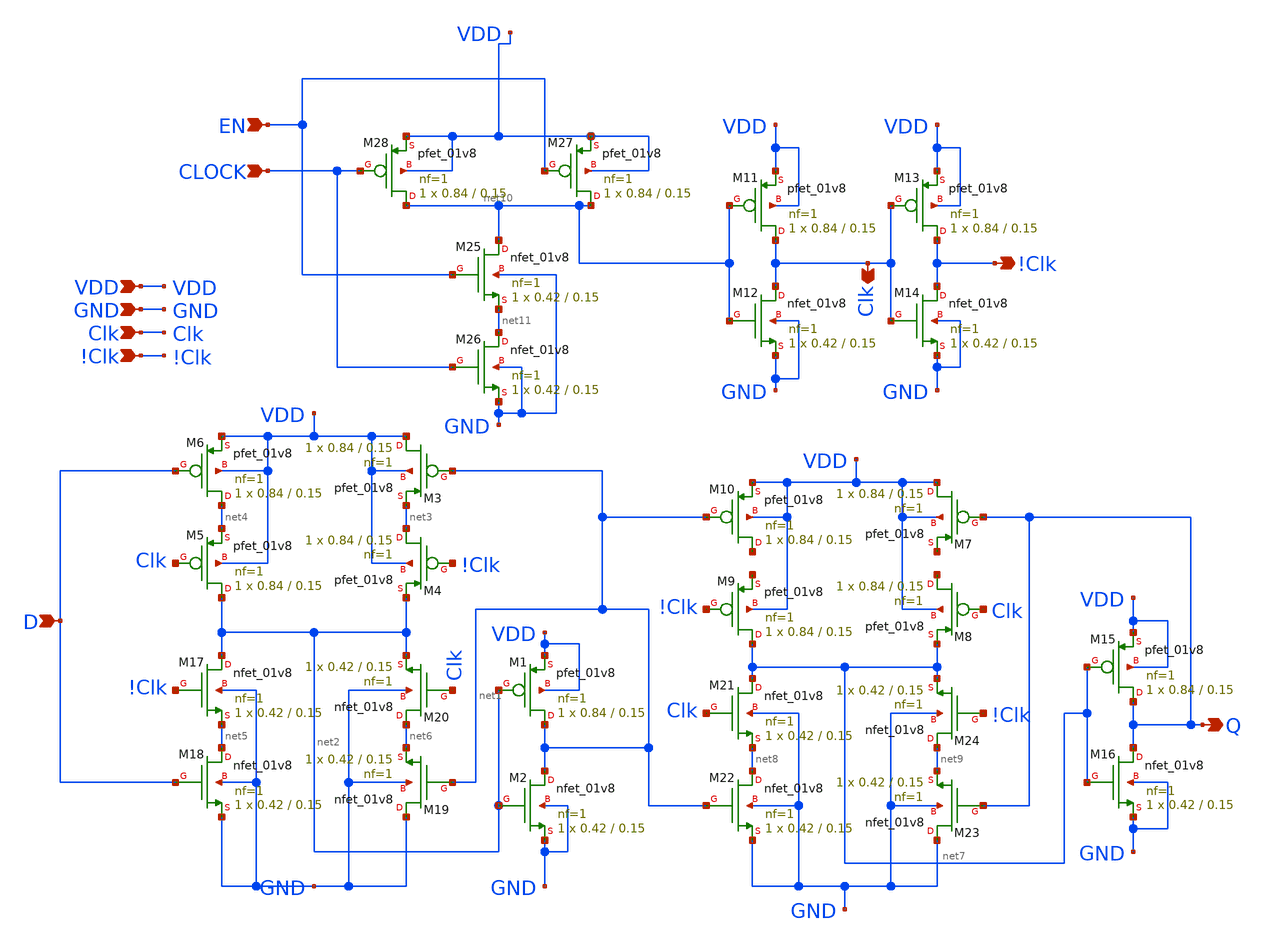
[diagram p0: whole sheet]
** sch_path: FF/xschem/DFF_EN.sch
**.subckt DFF_EN VDD GND Clk D Q Clk !Clk !Clk EN CLOCK
*.ipin VDD
*.ipin GND
*.ipin Clk
*.ipin D
*.opin Q
*.opin Clk
*.opin !Clk
*.ipin !Clk
*.ipin EN
*.ipin CLOCK
XM1 net1 net2 VDD VDD sky130_fd_pr__pfet_01v8 L=0.15 W=0.84 nf=1 ad='int((nf+1)/2) * W/nf * 0.29' as='int((nf+2)/2) * W/nf * 0.29'
+ pd='2*int((nf+1)/2) * (W/nf + 0.29)' ps='2*int((nf+2)/2) * (W/nf + 0.29)' nrd='0.29 / W' nrs='0.29 / W'
+ sa=0 sb=0 sd=0 mult=1 m=1
XM2 net1 net2 GND GND sky130_fd_pr__nfet_01v8 L=0.15 W=0.42 nf=1 ad='int((nf+1)/2) * W/nf * 0.29' as='int((nf+2)/2) * W/nf * 0.29'
+ pd='2*int((nf+1)/2) * (W/nf + 0.29)' ps='2*int((nf+2)/2) * (W/nf + 0.29)' nrd='0.29 / W' nrs='0.29 / W'
+ sa=0 sb=0 sd=0 mult=1 m=1
XM3 VDD net1 net3 VDD sky130_fd_pr__pfet_01v8 L=0.15 W=0.84 nf=1 ad='int((nf+1)/2) * W/nf * 0.29' as='int((nf+2)/2) * W/nf * 0.29'
+ pd='2*int((nf+1)/2) * (W/nf + 0.29)' ps='2*int((nf+2)/2) * (W/nf + 0.29)' nrd='0.29 / W' nrs='0.29 / W'
+ sa=0 sb=0 sd=0 mult=1 m=1
XM4 net3 !Clk net2 VDD sky130_fd_pr__pfet_01v8 L=0.15 W=0.84 nf=1 ad='int((nf+1)/2) * W/nf * 0.29' as='int((nf+2)/2) * W/nf * 0.29'
+ pd='2*int((nf+1)/2) * (W/nf + 0.29)' ps='2*int((nf+2)/2) * (W/nf + 0.29)' nrd='0.29 / W' nrs='0.29 / W'
+ sa=0 sb=0 sd=0 mult=1 m=1
XM5 net2 Clk net4 VDD sky130_fd_pr__pfet_01v8 L=0.15 W=0.84 nf=1 ad='int((nf+1)/2) * W/nf * 0.29' as='int((nf+2)/2) * W/nf * 0.29'
+ pd='2*int((nf+1)/2) * (W/nf + 0.29)' ps='2*int((nf+2)/2) * (W/nf + 0.29)' nrd='0.29 / W' nrs='0.29 / W'
+ sa=0 sb=0 sd=0 mult=1 m=1
XM6 net4 D VDD VDD sky130_fd_pr__pfet_01v8 L=0.15 W=0.84 nf=1 ad='int((nf+1)/2) * W/nf * 0.29' as='int((nf+2)/2) * W/nf * 0.29'
+ pd='2*int((nf+1)/2) * (W/nf + 0.29)' ps='2*int((nf+2)/2) * (W/nf + 0.29)' nrd='0.29 / W' nrs='0.29 / W'
+ sa=0 sb=0 sd=0 mult=1 m=1
XM7 VDD Q net12 VDD sky130_fd_pr__pfet_01v8 L=0.15 W=0.84 nf=1 ad='int((nf+1)/2) * W/nf * 0.29' as='int((nf+2)/2) * W/nf * 0.29'
+ pd='2*int((nf+1)/2) * (W/nf + 0.29)' ps='2*int((nf+2)/2) * (W/nf + 0.29)' nrd='0.29 / W' nrs='0.29 / W'
+ sa=0 sb=0 sd=0 mult=1 m=1
XM8 net13 Clk net7 VDD sky130_fd_pr__pfet_01v8 L=0.15 W=0.84 nf=1 ad='int((nf+1)/2) * W/nf * 0.29' as='int((nf+2)/2) * W/nf * 0.29'
+ pd='2*int((nf+1)/2) * (W/nf + 0.29)' ps='2*int((nf+2)/2) * (W/nf + 0.29)' nrd='0.29 / W' nrs='0.29 / W'
+ sa=0 sb=0 sd=0 mult=1 m=1
XM9 net7 !Clk net14 VDD sky130_fd_pr__pfet_01v8 L=0.15 W=0.84 nf=1 ad='int((nf+1)/2) * W/nf * 0.29' as='int((nf+2)/2) * W/nf * 0.29'
+ pd='2*int((nf+1)/2) * (W/nf + 0.29)' ps='2*int((nf+2)/2) * (W/nf + 0.29)' nrd='0.29 / W' nrs='0.29 / W'
+ sa=0 sb=0 sd=0 mult=1 m=1
XM10 net15 net1 VDD VDD sky130_fd_pr__pfet_01v8 L=0.15 W=0.84 nf=1 ad='int((nf+1)/2) * W/nf * 0.29' as='int((nf+2)/2) * W/nf * 0.29'
+ pd='2*int((nf+1)/2) * (W/nf + 0.29)' ps='2*int((nf+2)/2) * (W/nf + 0.29)' nrd='0.29 / W' nrs='0.29 / W'
+ sa=0 sb=0 sd=0 mult=1 m=1
XM11 Clk net10 VDD VDD sky130_fd_pr__pfet_01v8 L=0.15 W=0.84 nf=1 ad='int((nf+1)/2) * W/nf * 0.29' as='int((nf+2)/2) * W/nf * 0.29'
+ pd='2*int((nf+1)/2) * (W/nf + 0.29)' ps='2*int((nf+2)/2) * (W/nf + 0.29)' nrd='0.29 / W' nrs='0.29 / W'
+ sa=0 sb=0 sd=0 mult=1 m=1
XM12 Clk net10 GND GND sky130_fd_pr__nfet_01v8 L=0.15 W=0.42 nf=1 ad='int((nf+1)/2) * W/nf * 0.29' as='int((nf+2)/2) * W/nf * 0.29'
+ pd='2*int((nf+1)/2) * (W/nf + 0.29)' ps='2*int((nf+2)/2) * (W/nf + 0.29)' nrd='0.29 / W' nrs='0.29 / W'
+ sa=0 sb=0 sd=0 mult=1 m=1
XM13 !Clk Clk VDD VDD sky130_fd_pr__pfet_01v8 L=0.15 W=0.84 nf=1 ad='int((nf+1)/2) * W/nf * 0.29' as='int((nf+2)/2) * W/nf * 0.29'
+ pd='2*int((nf+1)/2) * (W/nf + 0.29)' ps='2*int((nf+2)/2) * (W/nf + 0.29)' nrd='0.29 / W' nrs='0.29 / W'
+ sa=0 sb=0 sd=0 mult=1 m=1
XM14 !Clk Clk GND GND sky130_fd_pr__nfet_01v8 L=0.15 W=0.42 nf=1 ad='int((nf+1)/2) * W/nf * 0.29' as='int((nf+2)/2) * W/nf * 0.29'
+ pd='2*int((nf+1)/2) * (W/nf + 0.29)' ps='2*int((nf+2)/2) * (W/nf + 0.29)' nrd='0.29 / W' nrs='0.29 / W'
+ sa=0 sb=0 sd=0 mult=1 m=1
XM15 Q net7 VDD VDD sky130_fd_pr__pfet_01v8 L=0.15 W=0.84 nf=1 ad='int((nf+1)/2) * W/nf * 0.29' as='int((nf+2)/2) * W/nf * 0.29'
+ pd='2*int((nf+1)/2) * (W/nf + 0.29)' ps='2*int((nf+2)/2) * (W/nf + 0.29)' nrd='0.29 / W' nrs='0.29 / W'
+ sa=0 sb=0 sd=0 mult=1 m=1
XM16 Q net7 GND GND sky130_fd_pr__nfet_01v8 L=0.15 W=0.42 nf=1 ad='int((nf+1)/2) * W/nf * 0.29' as='int((nf+2)/2) * W/nf * 0.29'
+ pd='2*int((nf+1)/2) * (W/nf + 0.29)' ps='2*int((nf+2)/2) * (W/nf + 0.29)' nrd='0.29 / W' nrs='0.29 / W'
+ sa=0 sb=0 sd=0 mult=1 m=1
XM17 net2 !Clk net5 GND sky130_fd_pr__nfet_01v8 L=0.15 W=0.42 nf=1 ad='int((nf+1)/2) * W/nf * 0.29' as='int((nf+2)/2) * W/nf * 0.29'
+ pd='2*int((nf+1)/2) * (W/nf + 0.29)' ps='2*int((nf+2)/2) * (W/nf + 0.29)' nrd='0.29 / W' nrs='0.29 / W'
+ sa=0 sb=0 sd=0 mult=1 m=1
XM18 net5 D GND GND sky130_fd_pr__nfet_01v8 L=0.15 W=0.42 nf=1 ad='int((nf+1)/2) * W/nf * 0.29' as='int((nf+2)/2) * W/nf * 0.29'
+ pd='2*int((nf+1)/2) * (W/nf + 0.29)' ps='2*int((nf+2)/2) * (W/nf + 0.29)' nrd='0.29 / W' nrs='0.29 / W'
+ sa=0 sb=0 sd=0 mult=1 m=1
XM19 GND net1 net6 GND sky130_fd_pr__nfet_01v8 L=0.15 W=0.42 nf=1 ad='int((nf+1)/2) * W/nf * 0.29' as='int((nf+2)/2) * W/nf * 0.29'
+ pd='2*int((nf+1)/2) * (W/nf + 0.29)' ps='2*int((nf+2)/2) * (W/nf + 0.29)' nrd='0.29 / W' nrs='0.29 / W'
+ sa=0 sb=0 sd=0 mult=1 m=1
XM20 net6 Clk net2 GND sky130_fd_pr__nfet_01v8 L=0.15 W=0.42 nf=1 ad='int((nf+1)/2) * W/nf * 0.29' as='int((nf+2)/2) * W/nf * 0.29'
+ pd='2*int((nf+1)/2) * (W/nf + 0.29)' ps='2*int((nf+2)/2) * (W/nf + 0.29)' nrd='0.29 / W' nrs='0.29 / W'
+ sa=0 sb=0 sd=0 mult=1 m=1
XM21 net7 Clk net8 GND sky130_fd_pr__nfet_01v8 L=0.15 W=0.42 nf=1 ad='int((nf+1)/2) * W/nf * 0.29' as='int((nf+2)/2) * W/nf * 0.29'
+ pd='2*int((nf+1)/2) * (W/nf + 0.29)' ps='2*int((nf+2)/2) * (W/nf + 0.29)' nrd='0.29 / W' nrs='0.29 / W'
+ sa=0 sb=0 sd=0 mult=1 m=1
XM22 net8 net1 GND GND sky130_fd_pr__nfet_01v8 L=0.15 W=0.42 nf=1 ad='int((nf+1)/2) * W/nf * 0.29' as='int((nf+2)/2) * W/nf * 0.29'
+ pd='2*int((nf+1)/2) * (W/nf + 0.29)' ps='2*int((nf+2)/2) * (W/nf + 0.29)' nrd='0.29 / W' nrs='0.29 / W'
+ sa=0 sb=0 sd=0 mult=1 m=1
XM23 GND Q net9 GND sky130_fd_pr__nfet_01v8 L=0.15 W=0.42 nf=1 ad='int((nf+1)/2) * W/nf * 0.29' as='int((nf+2)/2) * W/nf * 0.29'
+ pd='2*int((nf+1)/2) * (W/nf + 0.29)' ps='2*int((nf+2)/2) * (W/nf + 0.29)' nrd='0.29 / W' nrs='0.29 / W'
+ sa=0 sb=0 sd=0 mult=1 m=1
XM24 net9 !Clk net7 GND sky130_fd_pr__nfet_01v8 L=0.15 W=0.42 nf=1 ad='int((nf+1)/2) * W/nf * 0.29' as='int((nf+2)/2) * W/nf * 0.29'
+ pd='2*int((nf+1)/2) * (W/nf + 0.29)' ps='2*int((nf+2)/2) * (W/nf + 0.29)' nrd='0.29 / W' nrs='0.29 / W'
+ sa=0 sb=0 sd=0 mult=1 m=1
XM25 net10 EN net11 GND sky130_fd_pr__nfet_01v8 L=0.15 W=0.42 nf=1 ad='int((nf+1)/2) * W/nf * 0.29' as='int((nf+2)/2) * W/nf * 0.29'
+ pd='2*int((nf+1)/2) * (W/nf + 0.29)' ps='2*int((nf+2)/2) * (W/nf + 0.29)' nrd='0.29 / W' nrs='0.29 / W'
+ sa=0 sb=0 sd=0 mult=1 m=1
XM26 net11 CLOCK GND GND sky130_fd_pr__nfet_01v8 L=0.15 W=0.42 nf=1 ad='int((nf+1)/2) * W/nf * 0.29'
+ as='int((nf+2)/2) * W/nf * 0.29' pd='2*int((nf+1)/2) * (W/nf + 0.29)' ps='2*int((nf+2)/2) * (W/nf + 0.29)'
+ nrd='0.29 / W' nrs='0.29 / W' sa=0 sb=0 sd=0 mult=1 m=1
XM27 net10 EN VDD VDD sky130_fd_pr__pfet_01v8 L=0.15 W=0.84 nf=1 ad='int((nf+1)/2) * W/nf * 0.29' as='int((nf+2)/2) * W/nf * 0.29'
+ pd='2*int((nf+1)/2) * (W/nf + 0.29)' ps='2*int((nf+2)/2) * (W/nf + 0.29)' nrd='0.29 / W' nrs='0.29 / W'
+ sa=0 sb=0 sd=0 mult=1 m=1
XM28 net10 CLOCK VDD VDD sky130_fd_pr__pfet_01v8 L=0.15 W=0.84 nf=1 ad='int((nf+1)/2) * W/nf * 0.29'
+ as='int((nf+2)/2) * W/nf * 0.29' pd='2*int((nf+1)/2) * (W/nf + 0.29)' ps='2*int((nf+2)/2) * (W/nf + 0.29)'
+ nrd='0.29 / W' nrs='0.29 / W' sa=0 sb=0 sd=0 mult=1 m=1
**.ends
.end
